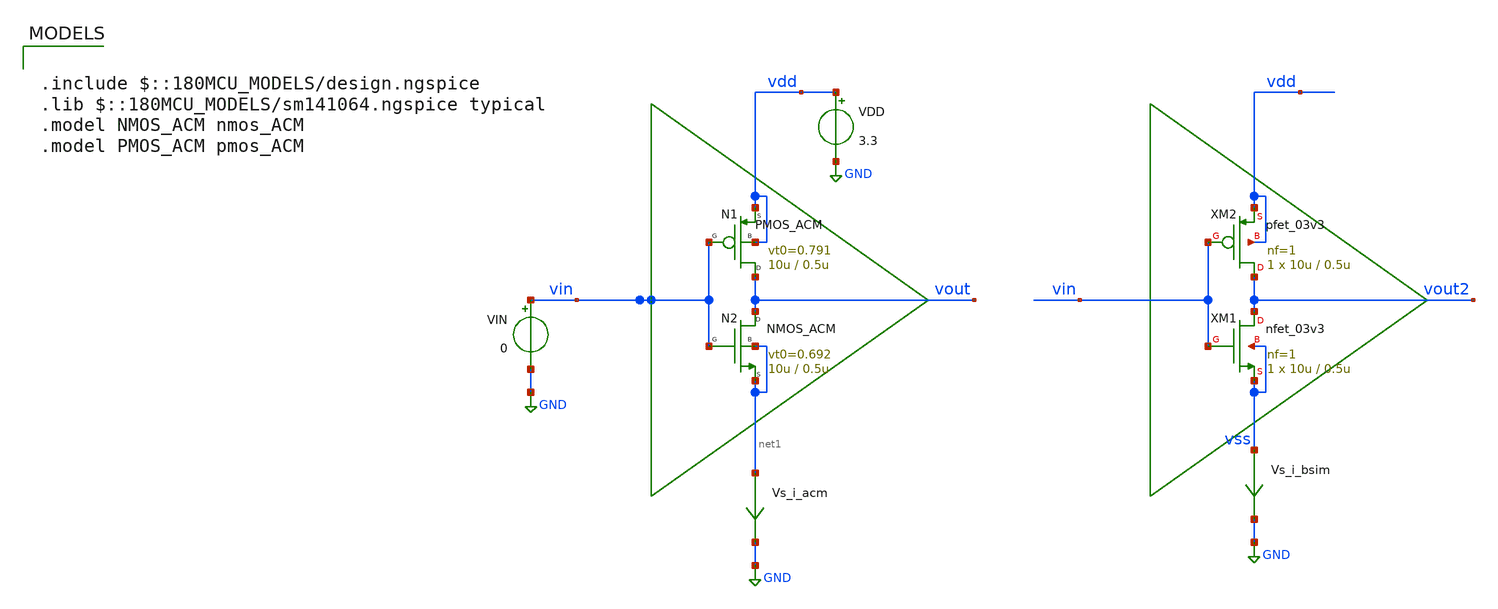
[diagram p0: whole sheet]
** sch_path: Examples/GF180MCU/xschem/TB_inv_acm_vt0.sch
**.subckt TB_inv_acm_vt0
VIN vin GND 0
VDD vdd GND 3.3
N2 vout vin net1 net1 NMOS_ACM w=10u l=0.5u n=1.37 is=1.33u vt0=0.692 sigma=6.1m zeta=0.1m
N1 vout vin vdd vdd PMOS_ACM w=10u l=0.5u n=1.42 is=0.41u vt0=0.791 sigma=6.1m zeta=0.1m
Vs_i_bsim vss GND 0
.save i(vs_i_bsim)
XM1 vout2 vin vss vss nfet_03v3 L=0.5u W=10u nf=1 ad='int((nf+1)/2) * W/nf * 0.18u' as='int((nf+2)/2) * W/nf * 0.18u'
+ pd='2*int((nf+1)/2) * (W/nf + 0.18u)' ps='2*int((nf+2)/2) * (W/nf + 0.18u)' nrd='0.18u / W' nrs='0.18u / W'
+ sa=0 sb=0 sd=0 m=1
XM2 vout2 vin vdd vdd pfet_03v3 L=0.5u W=10u nf=1 ad='int((nf+1)/2) * W/nf * 0.18u' as='int((nf+2)/2) * W/nf * 0.18u'
+ pd='2*int((nf+1)/2) * (W/nf + 0.18u)' ps='2*int((nf+2)/2) * (W/nf + 0.18u)' nrd='0.18u / W' nrs='0.18u / W'
+ sa=0 sb=0 sd=0 m=1
Vs_i_acm net1 GND 0
.save i(vs_i_acm)
**** begin user architecture code

.include $::180MCU_MODELS/design.ngspice
.lib $::180MCU_MODELS/sm141064.ngspice typical
.model NMOS_ACM nmos_ACM
.model PMOS_ACM pmos_ACM



*.option gmin=1e-18
.control
pre_osdi /home/gmaranhao/Documents/MOSFET_model/Examples/GF180MCU/xschem/symbol/NMOS_ACM_2V0.osdi
pre_osdi /home/gmaranhao/Documents/MOSFET_model/Examples/GF180MCU/xschem/symbol/PMOS_ACM_2V0.osdi
save all

op
remzerovec
write TB_inv_acm_vt0.raw
set appendwrite

dc VIN 0 3.3 1m
remzerovec
write TB_inv_acm_vt0.raw
set appendwrite

.endc


**** end user architecture code
**.ends
.GLOBAL GND
.end
